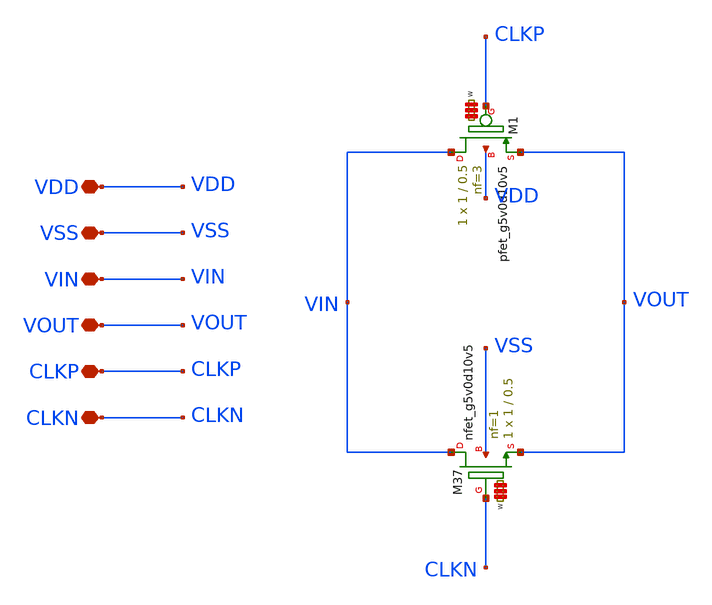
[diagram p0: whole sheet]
** sch_path: LIB/Sky130A/switches/passgate.sch
**.subckt passgate VDD VSS VIN VOUT CLKP CLKN
*.iopin VDD
*.iopin VSS
*.iopin VIN
*.iopin VOUT
*.iopin CLKP
*.iopin CLKN
XM1 VIN CLKP VOUT VDD sky130_fd_pr__pfet_g5v0d10v5 L=0.5 W='1 * 3 ' nf=3 ad='int((3 + 1)/2) * 1 * 0.29'
+ as='int((3 + 2)/2) * 1 * 0.29' pd='2*int((3 + 1)/2) * (1 + 0.29)' ps='2*int((3 + 2)/2) * (1 + 0.29)'
+ nrd='0.29 / 1 / 3 ' nrs='0.29 / 1 / 3 ' sa=0 sb=0 sd=0 mult=1 m=1
XM37 VIN CLKN VOUT VSS sky130_fd_pr__nfet_g5v0d10v5 L=0.5 W='1 * 1 ' nf=1 ad='int((nf+1)/2) * W / nf * 0.29'
+ as='int((nf+2)/2) * W / nf * 0.29' pd='2*int((nf+1)/2) * (W / nf + 0.29)' ps='2*int((nf+2)/2) * (W / nf + 0.29)'
+ nrd='0.29 / W ' nrs='0.29 / W ' sa=0 sb=0 sd=0 mult=1 m=1
**.ends
.end
